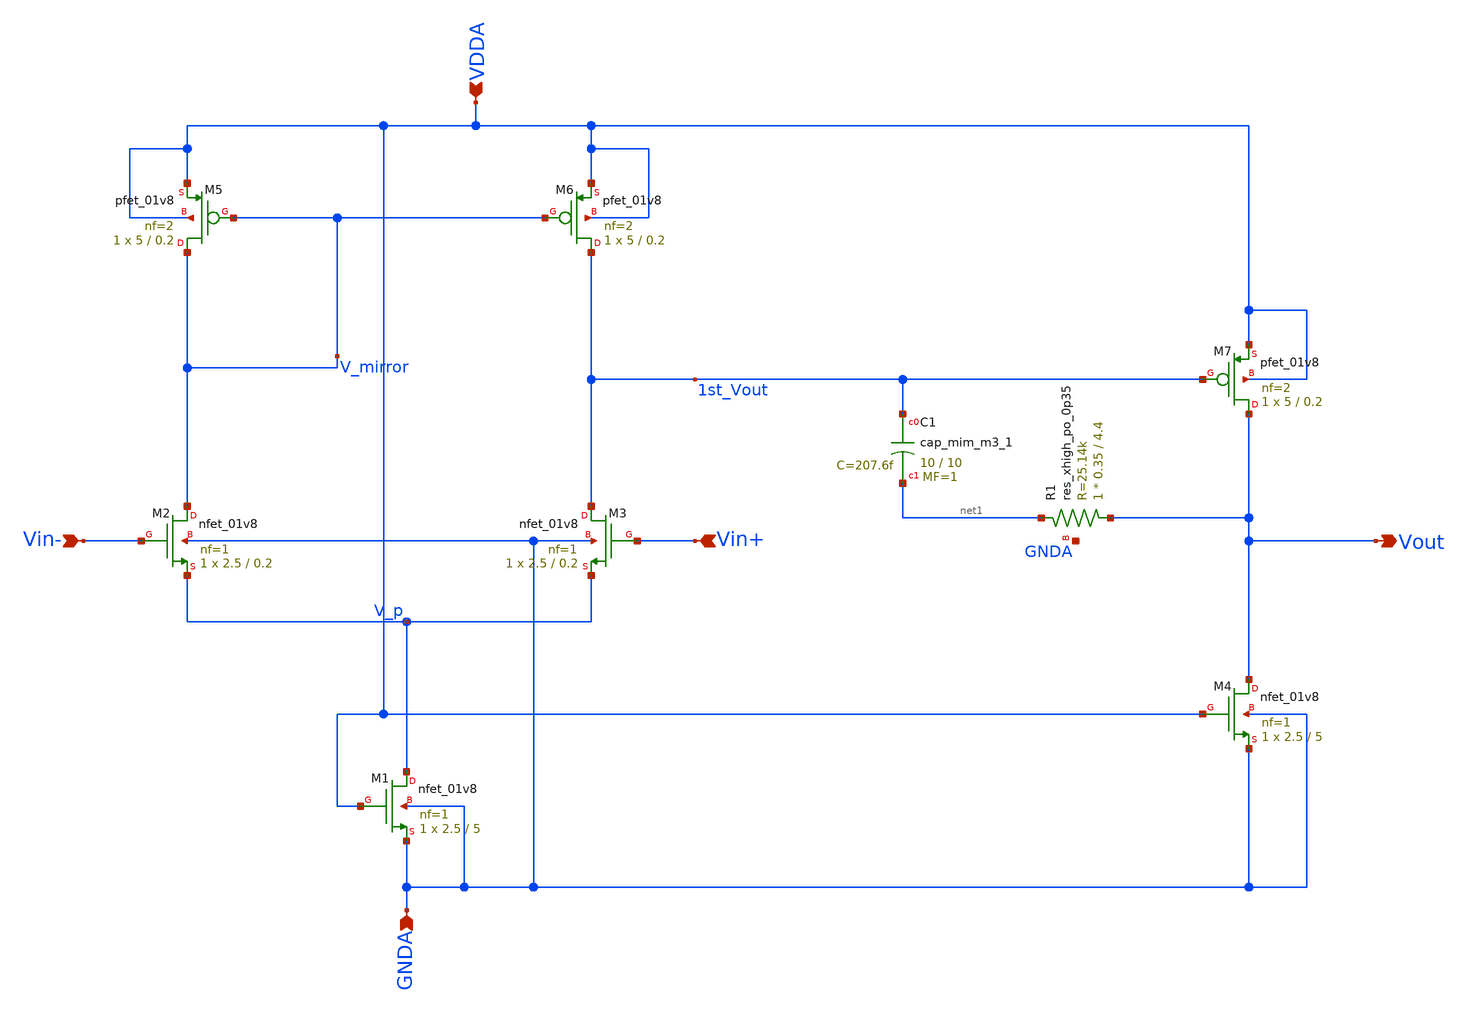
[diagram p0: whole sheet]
** sch_path: projects/bandgapref/xschem_ngspice/new_files/opamp_bandgap_2.sch
**.subckt opamp_bandgap_2 Vin+ Vout Vin- GNDA VDDA
*.ipin Vin+
*.opin Vout
*.ipin Vin-
*.ipin GNDA
*.ipin VDDA
XM1 V_p VDDA GNDA GNDA sky130_fd_pr__nfet_01v8 L=5 W=2.5 nf=1 ad='int((nf+1)/2) * W/nf * 0.29' as='int((nf+2)/2) * W/nf * 0.29'
+ pd='2*int((nf+1)/2) * (W/nf + 0.29)' ps='2*int((nf+2)/2) * (W/nf + 0.29)' nrd='0.29 / W' nrs='0.29 / W'
+ sa=0 sb=0 sd=0 mult=1 m=1
XM2 V_mirror Vin- V_p GNDA sky130_fd_pr__nfet_01v8 L=0.2 W=2.5 nf=1 ad='int((nf+1)/2) * W/nf * 0.29'
+ as='int((nf+2)/2) * W/nf * 0.29' pd='2*int((nf+1)/2) * (W/nf + 0.29)' ps='2*int((nf+2)/2) * (W/nf + 0.29)'
+ nrd='0.29 / W' nrs='0.29 / W' sa=0 sb=0 sd=0 mult=1 m=1
XM3 1st_Vout Vin+ V_p GNDA sky130_fd_pr__nfet_01v8 L=0.2 W=2.5 nf=1 ad='int((nf+1)/2) * W/nf * 0.29'
+ as='int((nf+2)/2) * W/nf * 0.29' pd='2*int((nf+1)/2) * (W/nf + 0.29)' ps='2*int((nf+2)/2) * (W/nf + 0.29)'
+ nrd='0.29 / W' nrs='0.29 / W' sa=0 sb=0 sd=0 mult=1 m=1
XM5 V_mirror V_mirror VDDA VDDA sky130_fd_pr__pfet_01v8 L=0.2 W=5 nf=2 ad='int((nf+1)/2) * W/nf * 0.29'
+ as='int((nf+2)/2) * W/nf * 0.29' pd='2*int((nf+1)/2) * (W/nf + 0.29)' ps='2*int((nf+2)/2) * (W/nf + 0.29)'
+ nrd='0.29 / W' nrs='0.29 / W' sa=0 sb=0 sd=0 mult=1 m=1
XM6 1st_Vout V_mirror VDDA VDDA sky130_fd_pr__pfet_01v8 L=0.2 W=5 nf=2 ad='int((nf+1)/2) * W/nf * 0.29'
+ as='int((nf+2)/2) * W/nf * 0.29' pd='2*int((nf+1)/2) * (W/nf + 0.29)' ps='2*int((nf+2)/2) * (W/nf + 0.29)'
+ nrd='0.29 / W' nrs='0.29 / W' sa=0 sb=0 sd=0 mult=1 m=1
XM4 Vout VDDA GNDA GNDA sky130_fd_pr__nfet_01v8 L=5 W=2.5 nf=1 ad='int((nf+1)/2) * W/nf * 0.29' as='int((nf+2)/2) * W/nf * 0.29'
+ pd='2*int((nf+1)/2) * (W/nf + 0.29)' ps='2*int((nf+2)/2) * (W/nf + 0.29)' nrd='0.29 / W' nrs='0.29 / W'
+ sa=0 sb=0 sd=0 mult=1 m=1
XM7 Vout 1st_Vout VDDA VDDA sky130_fd_pr__pfet_01v8 L=0.2 W=5 nf=2 ad='int((nf+1)/2) * W/nf * 0.29' as='int((nf+2)/2) * W/nf * 0.29'
+ pd='2*int((nf+1)/2) * (W/nf + 0.29)' ps='2*int((nf+2)/2) * (W/nf + 0.29)' nrd='0.29 / W' nrs='0.29 / W'
+ sa=0 sb=0 sd=0 mult=1 m=1
XC1 1st_Vout net1 sky130_fd_pr__cap_mim_m3_1 W=10 L=10 MF=1 m=1
XR1 Vout net1 GNDA sky130_fd_pr__res_xhigh_po_0p35 L=4.4 mult=1 m=1
**.ends
.end
